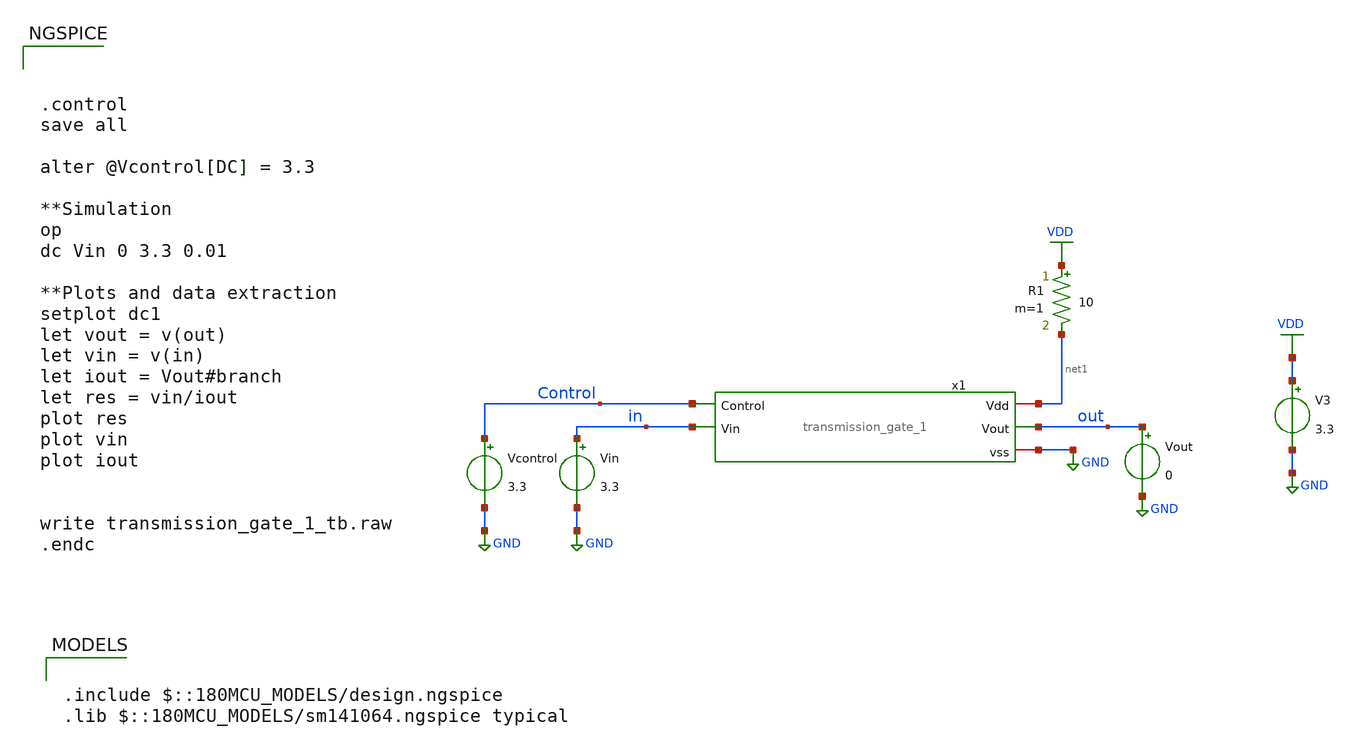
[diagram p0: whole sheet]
** sch_path: designs/libs/core_analog/Transmission_Gate/transmission_gate_1_tb.sch
**.subckt transmission_gate_1_tb
x1 net1 Control out in GND transmission_gate_1
Vin in GND 3.3
Vcontrol Control GND 3.3
V3 VDD GND 3.3
Vout out GND 0
R1 VDD net1 10 m=1
**** begin user architecture code

.include $::180MCU_MODELS/design.ngspice
.lib $::180MCU_MODELS/sm141064.ngspice typical




.control
save all

alter @Vcontrol[DC] = 3.3

**Simulation
op
dc Vin 0 3.3 0.01

**Plots and data extraction
setplot dc1
let vout = v(out)
let vin = v(in)
let iout = Vout#branch
let res = vin/iout
plot res
plot vin
plot iout


write transmission_gate_1_tb.raw
.endc


**** end user architecture code
**.ends

* expanding   symbol:  transmission_gate_1.sym # of pins=5
** sym_path: designs/libs/core_analog/Transmission_Gate/transmission_gate_1.sym
** sch_path: designs/libs/core_analog/Transmission_Gate/transmission_gate_1.sch
.subckt transmission_gate_1 Vdd Control Vout Vin vss
*.iopin Vdd
*.ipin Control
*.opin Vout
*.ipin Vin
*.iopin vss
XM1 net1 Control vss vss nfet_03v3 L=0.28u W=0.85u nf=1 ad='int((nf+1)/2) * W/nf * 0.18u' as='int((nf+2)/2) * W/nf * 0.18u'
+ pd='2*int((nf+1)/2) * (W/nf + 0.18u)' ps='2*int((nf+2)/2) * (W/nf + 0.18u)' nrd='0.18u / W' nrs='0.18u / W'
+ sa=0 sb=0 sd=0 m=1
XM2 net1 Control Vdd Vdd pfet_03v3 L=0.28u W=1.7u nf=1 ad='int((nf+1)/2) * W/nf * 0.18u' as='int((nf+2)/2) * W/nf * 0.18u'
+ pd='2*int((nf+1)/2) * (W/nf + 0.18u)' ps='2*int((nf+2)/2) * (W/nf + 0.18u)' nrd='0.18u / W' nrs='0.18u / W'
+ sa=0 sb=0 sd=0 m=1
XM3 Vout Control Vin vss nfet_03v3 L=0.28u W=2.4u nf=1 ad='int((nf+1)/2) * W/nf * 0.18u' as='int((nf+2)/2) * W/nf * 0.18u'
+ pd='2*int((nf+1)/2) * (W/nf + 0.18u)' ps='2*int((nf+2)/2) * (W/nf + 0.18u)' nrd='0.18u / W' nrs='0.18u / W'
+ sa=0 sb=0 sd=0 m=10
XM4 Vout net1 Vin Vdd pfet_03v3 L=0.28u W=7.2u nf=1 ad='int((nf+1)/2) * W/nf * 0.18u' as='int((nf+2)/2) * W/nf * 0.18u'
+ pd='2*int((nf+1)/2) * (W/nf + 0.18u)' ps='2*int((nf+2)/2) * (W/nf + 0.18u)' nrd='0.18u / W' nrs='0.18u / W'
+ sa=0 sb=0 sd=0 m=10
.ends

.GLOBAL VDD
.GLOBAL GND
.end
